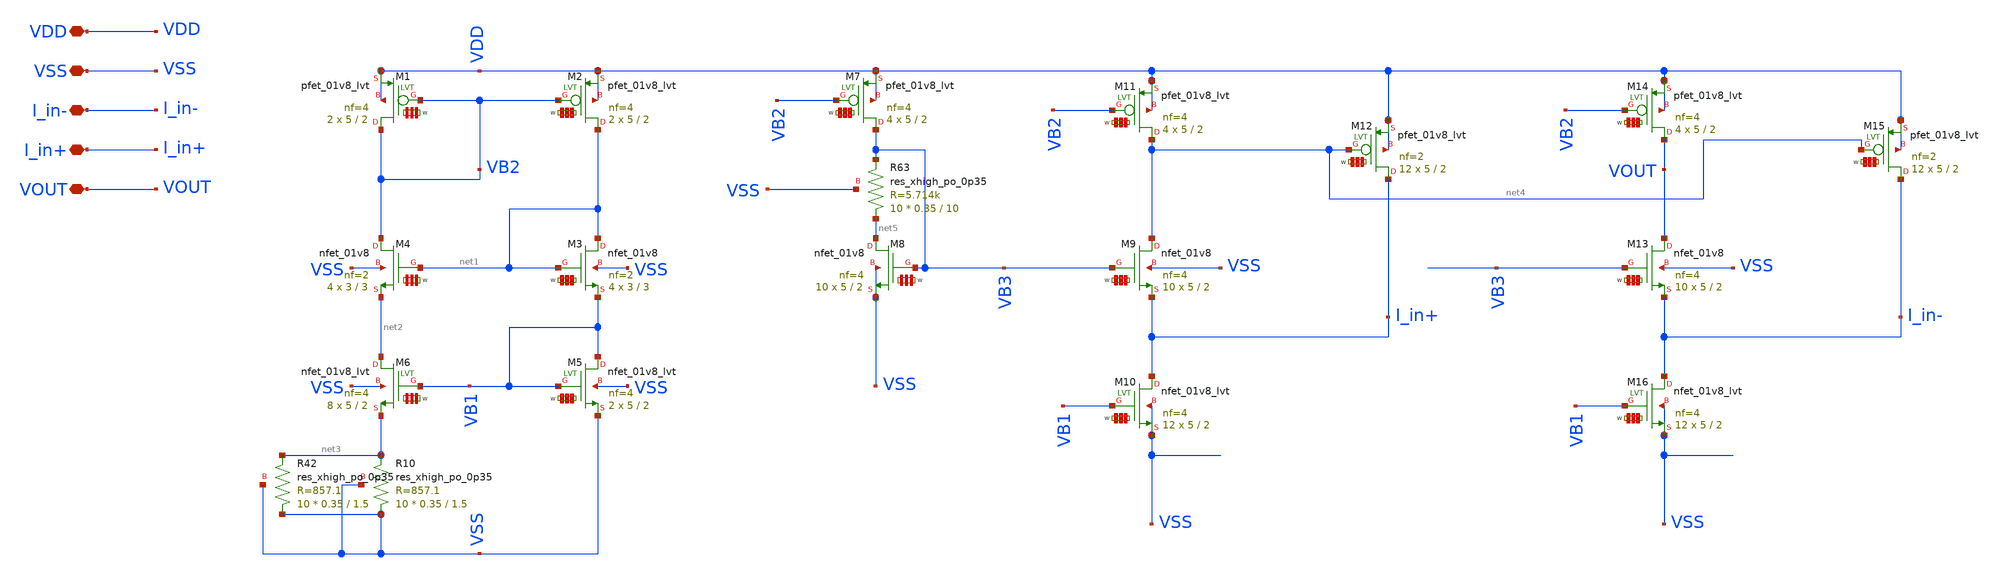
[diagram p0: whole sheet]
** sch_path: my_ip/sky130A/OTRA_VGA/OTRA.sch
**.subckt OTRA VDD VSS I_in- I_in+ VOUT
*.iopin VDD
*.iopin VSS
*.iopin I_in-
*.iopin I_in+
*.iopin VOUT
XM2 net1 VB2 VDD VDD sky130_fd_pr__pfet_01v8_lvt L=2 W='5 * 4 ' nf=4 ad='int((4 + 1)/2) * 5 / 4 * 0.29'
+ as='int((4 + 2)/2) * 5 / 4 * 0.29' pd='2*int((4 + 1)/2) * (5 / 4 + 0.29)' ps='2*int((4 + 2)/2) * (5 / 4 + 0.29)'
+ nrd='0.29 / 5 ' nrs='0.29 / 5 ' sa=0 sb=0 sd=0 mult=2 m=2
XM1 VB2 VB2 VDD VDD sky130_fd_pr__pfet_01v8_lvt L=2 W='5 * 4 ' nf=4 ad='int((4 + 1)/2) * 5 / 4 * 0.29'
+ as='int((4 + 2)/2) * 5 / 4 * 0.29' pd='2*int((4 + 1)/2) * (5 / 4 + 0.29)' ps='2*int((4 + 2)/2) * (5 / 4 + 0.29)'
+ nrd='0.29 / 5 ' nrs='0.29 / 5 ' sa=0 sb=0 sd=0 mult=2 m=2
XR10 VSS net3 VSS sky130_fd_pr__res_xhigh_po_0p35 L=1.5 mult=10 m=10
XM4 VB2 net1 net2 VSS sky130_fd_pr__nfet_01v8 L=3 W='3 * 2 ' nf=2 ad='int((2 + 1)/2) * 3 / 2 * 0.29'
+ as='int((2 + 2)/2) * 3 / 2 * 0.29' pd='2*int((2 + 1)/2) * (3 / 2 + 0.29)' ps='2*int((2 + 2)/2) * (3 / 2 + 0.29)'
+ nrd='0.29 / 3 ' nrs='0.29 / 3 ' sa=0 sb=0 sd=0 mult=4 m=4
XM3 net1 net1 VB1 VSS sky130_fd_pr__nfet_01v8 L=3 W='3 * 2 ' nf=2 ad='int((2 + 1)/2) * 3 / 2 * 0.29'
+ as='int((2 + 2)/2) * 3 / 2 * 0.29' pd='2*int((2 + 1)/2) * (3 / 2 + 0.29)' ps='2*int((2 + 2)/2) * (3 / 2 + 0.29)'
+ nrd='0.29 / 3 ' nrs='0.29 / 3 ' sa=0 sb=0 sd=0 mult=4 m=4
XM8 net5 VB3 VSS VSS sky130_fd_pr__nfet_01v8 L=2 W='5 * 4 ' nf=4 ad='int((4 + 1)/2) * 5 / 4 * 0.29' as='int((4 + 2)/2) * 5 / 4 * 0.29'
+ pd='2*int((4 + 1)/2) * (5 / 4 + 0.29)' ps='2*int((4 + 2)/2) * (5 / 4 + 0.29)' nrd='0.29 / 5 ' nrs='0.29 / 5 '
+ sa=0 sb=0 sd=0 mult=10 m=10
XM9 net4 VB3 I_in+ VSS sky130_fd_pr__nfet_01v8 L=2 W='5 * 4 ' nf=4 ad='int((4 + 1)/2) * 5 / 4 * 0.29'
+ as='int((4 + 2)/2) * 5 / 4 * 0.29' pd='2*int((4 + 1)/2) * (5 / 4 + 0.29)' ps='2*int((4 + 2)/2) * (5 / 4 + 0.29)'
+ nrd='0.29 / 5 ' nrs='0.29 / 5 ' sa=0 sb=0 sd=0 mult=10 m=10
XR42 VSS net3 VSS sky130_fd_pr__res_xhigh_po_0p35 L=1.5 mult=10 m=10
XM7 VB3 VB2 VDD VDD sky130_fd_pr__pfet_01v8_lvt L=2 W='5 * 4 ' nf=4 ad='int((4 + 1)/2) * 5 / 4 * 0.29'
+ as='int((4 + 2)/2) * 5 / 4 * 0.29' pd='2*int((4 + 1)/2) * (5 / 4 + 0.29)' ps='2*int((4 + 2)/2) * (5 / 4 + 0.29)'
+ nrd='0.29 / 5 ' nrs='0.29 / 5 ' sa=0 sb=0 sd=0 mult=4 m=4
XM11 net4 VB2 VDD VDD sky130_fd_pr__pfet_01v8_lvt L=2 W='5 * 4 ' nf=4 ad='int((4 + 1)/2) * 5 / 4 * 0.29'
+ as='int((4 + 2)/2) * 5 / 4 * 0.29' pd='2*int((4 + 1)/2) * (5 / 4 + 0.29)' ps='2*int((4 + 2)/2) * (5 / 4 + 0.29)'
+ nrd='0.29 / 5 ' nrs='0.29 / 5 ' sa=0 sb=0 sd=0 mult=4 m=4
XM12 I_in+ net4 VDD VDD sky130_fd_pr__pfet_01v8_lvt L=2 W='5 * 2 ' nf=2 ad='int((2 + 1)/2) * 5 / 2 * 0.29'
+ as='int((2 + 2)/2) * 5 / 2 * 0.29' pd='2*int((2 + 1)/2) * (5 / 2 + 0.29)' ps='2*int((2 + 2)/2) * (5 / 2 + 0.29)'
+ nrd='0.29 / 5 ' nrs='0.29 / 5 ' sa=0 sb=0 sd=0 mult=12 m=12
XR63 net5 VB3 VSS sky130_fd_pr__res_xhigh_po_0p35 L=10 mult=10 m=10
XM5 VB1 VB1 VSS VSS sky130_fd_pr__nfet_01v8_lvt L=2 W='5 * 4 ' nf=4 ad='int((4 + 1)/2) * 5 / 4 * 0.29'
+ as='int((4 + 2)/2) * 5 / 4 * 0.29' pd='2*int((4 + 1)/2) * (5 / 4 + 0.29)' ps='2*int((4 + 2)/2) * (5 / 4 + 0.29)'
+ nrd='0.29 / 5 ' nrs='0.29 / 5 ' sa=0 sb=0 sd=0 mult=2 m=2
XM6 net2 VB1 net3 VSS sky130_fd_pr__nfet_01v8_lvt L=2 W='5 * 4 ' nf=4 ad='int((4 + 1)/2) * 5 / 4 * 0.29'
+ as='int((4 + 2)/2) * 5 / 4 * 0.29' pd='2*int((4 + 1)/2) * (5 / 4 + 0.29)' ps='2*int((4 + 2)/2) * (5 / 4 + 0.29)'
+ nrd='0.29 / 5 ' nrs='0.29 / 5 ' sa=0 sb=0 sd=0 mult=8 m=8
XM10 I_in+ VB1 VSS VSS sky130_fd_pr__nfet_01v8_lvt L=2 W='5 * 4 ' nf=4 ad='int((4 + 1)/2) * 5 / 4 * 0.29'
+ as='int((4 + 2)/2) * 5 / 4 * 0.29' pd='2*int((4 + 1)/2) * (5 / 4 + 0.29)' ps='2*int((4 + 2)/2) * (5 / 4 + 0.29)'
+ nrd='0.29 / 5 ' nrs='0.29 / 5 ' sa=0 sb=0 sd=0 mult=12 m=12
XM13 VOUT VB3 I_in- VSS sky130_fd_pr__nfet_01v8 L=2 W='5 * 4 ' nf=4 ad='int((4 + 1)/2) * 5 / 4 * 0.29'
+ as='int((4 + 2)/2) * 5 / 4 * 0.29' pd='2*int((4 + 1)/2) * (5 / 4 + 0.29)' ps='2*int((4 + 2)/2) * (5 / 4 + 0.29)'
+ nrd='0.29 / 5 ' nrs='0.29 / 5 ' sa=0 sb=0 sd=0 mult=10 m=10
XM14 VOUT VB2 VDD VDD sky130_fd_pr__pfet_01v8_lvt L=2 W='5 * 4 ' nf=4 ad='int((4 + 1)/2) * 5 / 4 * 0.29'
+ as='int((4 + 2)/2) * 5 / 4 * 0.29' pd='2*int((4 + 1)/2) * (5 / 4 + 0.29)' ps='2*int((4 + 2)/2) * (5 / 4 + 0.29)'
+ nrd='0.29 / 5 ' nrs='0.29 / 5 ' sa=0 sb=0 sd=0 mult=4 m=4
XM15 I_in- net4 VDD VDD sky130_fd_pr__pfet_01v8_lvt L=2 W='5 * 2 ' nf=2 ad='int((2 + 1)/2) * 5 / 2 * 0.29'
+ as='int((2 + 2)/2) * 5 / 2 * 0.29' pd='2*int((2 + 1)/2) * (5 / 2 + 0.29)' ps='2*int((2 + 2)/2) * (5 / 2 + 0.29)'
+ nrd='0.29 / 5 ' nrs='0.29 / 5 ' sa=0 sb=0 sd=0 mult=12 m=12
XM16 I_in- VB1 VSS VSS sky130_fd_pr__nfet_01v8_lvt L=2 W='5 * 4 ' nf=4 ad='int((4 + 1)/2) * 5 / 4 * 0.29'
+ as='int((4 + 2)/2) * 5 / 4 * 0.29' pd='2*int((4 + 1)/2) * (5 / 4 + 0.29)' ps='2*int((4 + 2)/2) * (5 / 4 + 0.29)'
+ nrd='0.29 / 5 ' nrs='0.29 / 5 ' sa=0 sb=0 sd=0 mult=12 m=12
**.ends
.end
